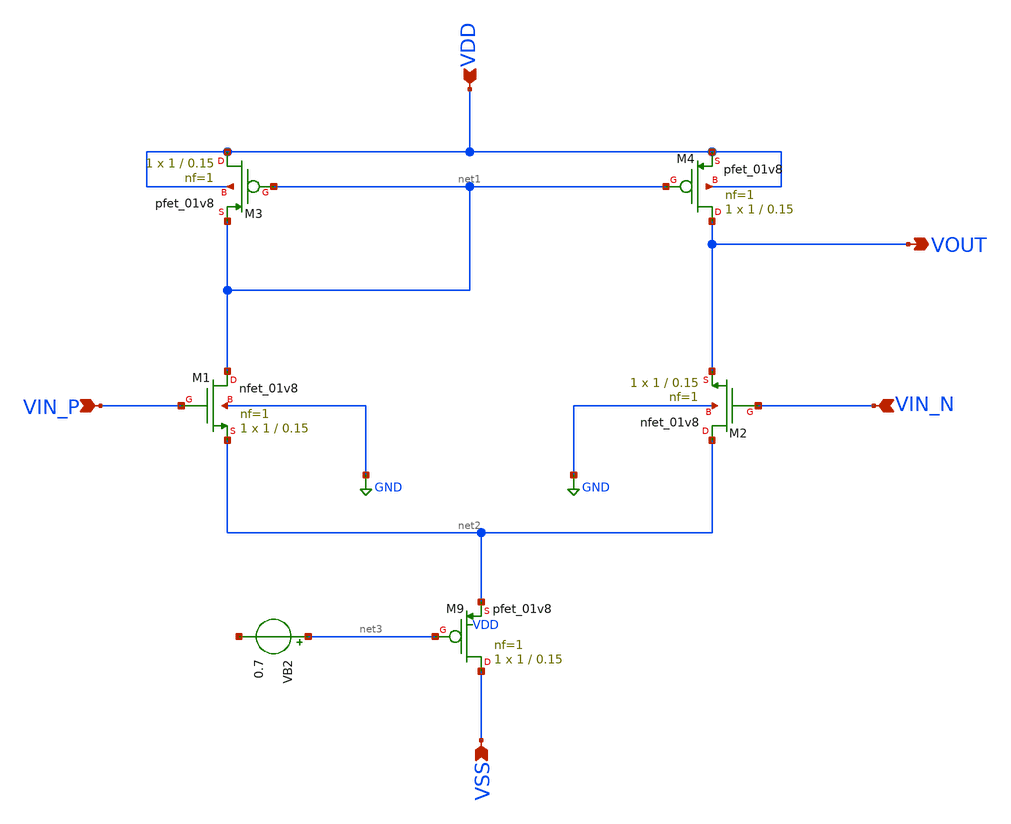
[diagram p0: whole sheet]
** sch_path: analog/schematics/opamp_single_stage.sch
**.subckt opamp_single_stage VIN_P VIN_N VDD VSS VOUT
*.ipin VIN_P
*.ipin VIN_N
*.ipin VDD
*.ipin VSS
*.opin VOUT
XM1 net1 VIN_P net2 GND sky130_fd_pr__nfet_01v8 L=0.15 W=1 nf=1 ad='int((1 + 1)/2) * 1 / 1 * 0.29' as='int((1 + 2)/2) * 1 / 1 * 0.29'
+ pd='2*int((1 + 1)/2) * (1 / 1 + 0.29)' ps='2*int((1 + 2)/2) * (1 / 1 + 0.29)' nrd='0.29 / 1 ' nrs='0.29 / 1 '
+ sa=0 sb=0 sd=0 mult=1 m=1
XM9 VSS net3 net2 VDD sky130_fd_pr__pfet_01v8 L=0.15 W=1 nf=1 ad='int((1 + 1)/2) * 1 / 1 * 0.29' as='int((1 + 2)/2) * 1 / 1 * 0.29'
+ pd='2*int((1 + 1)/2) * (1 / 1 + 0.29)' ps='2*int((1 + 2)/2) * (1 / 1 + 0.29)' nrd='0.29 / 1 ' nrs='0.29 / 1 '
+ sa=0 sb=0 sd=0 mult=1 m=1
XM2 net2 VIN_N VOUT GND sky130_fd_pr__nfet_01v8 L=0.15 W=1 nf=1 ad='int((1 + 1)/2) * 1 / 1 * 0.29' as='int((1 + 2)/2) * 1 / 1 * 0.29'
+ pd='2*int((1 + 1)/2) * (1 / 1 + 0.29)' ps='2*int((1 + 2)/2) * (1 / 1 + 0.29)' nrd='0.29 / 1 ' nrs='0.29 / 1 '
+ sa=0 sb=0 sd=0 mult=1 m=1
XM3 VDD net1 net1 VDD sky130_fd_pr__pfet_01v8 L=0.15 W=1 nf=1 ad='int((nf+1)/2) * W/nf * 0.29' as='int((nf+2)/2) * W/nf * 0.29'
+ pd='2*int((nf+1)/2) * (W/nf + 0.29)' ps='2*int((nf+2)/2) * (W/nf + 0.29)' nrd='0.29 / W' nrs='0.29 / W'
+ sa=0 sb=0 sd=0 mult=1 m=1
XM4 VOUT net1 VDD VDD sky130_fd_pr__pfet_01v8 L=0.15 W=1 nf=1 ad='int((nf+1)/2) * W/nf * 0.29' as='int((nf+2)/2) * W/nf * 0.29'
+ pd='2*int((nf+1)/2) * (W/nf + 0.29)' ps='2*int((nf+2)/2) * (W/nf + 0.29)' nrd='0.29 / W' nrs='0.29 / W'
+ sa=0 sb=0 sd=0 mult=1 m=1
VB2 net3 net4 0.7
**.ends
.GLOBAL GND
.end
